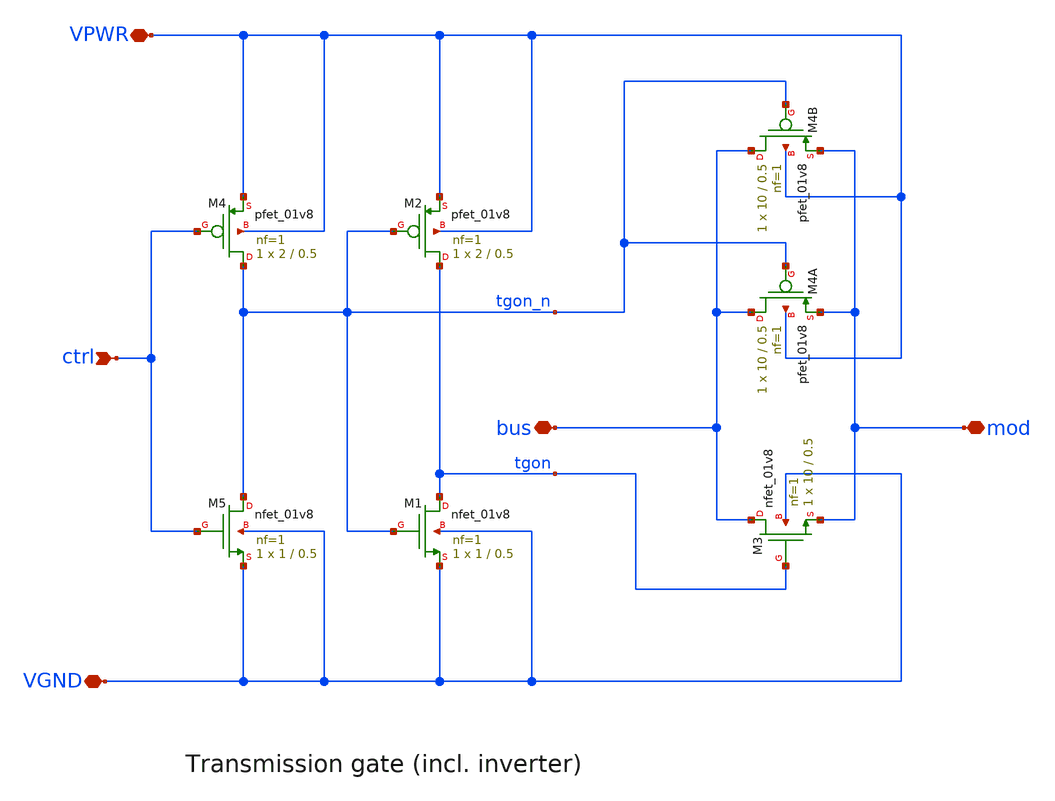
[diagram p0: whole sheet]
** sch_path: xschem/tt_asw_1v8.sch
**.subckt tt_asw_1v8 VPWR VGND mod bus ctrl
*.iopin VPWR
*.iopin VGND
*.iopin mod
*.iopin bus
*.ipin ctrl
XM3 bus tgon mod VGND sky130_fd_pr__nfet_01v8 L=0.5 W=10 nf=1 ad='int((nf+1)/2) * W/nf * 0.29' as='int((nf+2)/2) * W/nf * 0.29'
+ pd='2*int((nf+1)/2) * (W/nf + 0.29)' ps='2*int((nf+2)/2) * (W/nf + 0.29)' nrd='0.29 / W' nrs='0.29 / W'
+ sa=0 sb=0 sd=0 mult=1 m=1
XM4A bus tgon_n mod VPWR sky130_fd_pr__pfet_01v8 L=0.5 W=10 nf=1 ad='int((nf+1)/2) * W/nf * 0.29' as='int((nf+2)/2) * W/nf * 0.29'
+ pd='2*int((nf+1)/2) * (W/nf + 0.29)' ps='2*int((nf+2)/2) * (W/nf + 0.29)' nrd='0.29 / W' nrs='0.29 / W'
+ sa=0 sb=0 sd=0 mult=1 m=1
XM4B bus tgon_n mod VPWR sky130_fd_pr__pfet_01v8 L=0.5 W=10 nf=1 ad='int((nf+1)/2) * W/nf * 0.29' as='int((nf+2)/2) * W/nf * 0.29'
+ pd='2*int((nf+1)/2) * (W/nf + 0.29)' ps='2*int((nf+2)/2) * (W/nf + 0.29)' nrd='0.29 / W' nrs='0.29 / W'
+ sa=0 sb=0 sd=0 mult=1 m=1
XM1 tgon tgon_n VGND VGND sky130_fd_pr__nfet_01v8 L=0.5 W=1 nf=1 ad='int((nf+1)/2) * W/nf * 0.29' as='int((nf+2)/2) * W/nf * 0.29'
+ pd='2*int((nf+1)/2) * (W/nf + 0.29)' ps='2*int((nf+2)/2) * (W/nf + 0.29)' nrd='0.29 / W' nrs='0.29 / W'
+ sa=0 sb=0 sd=0 mult=1 m=1
XM2 tgon tgon_n VPWR VPWR sky130_fd_pr__pfet_01v8 L=0.5 W=2 nf=1 ad='int((nf+1)/2) * W/nf * 0.29' as='int((nf+2)/2) * W/nf * 0.29'
+ pd='2*int((nf+1)/2) * (W/nf + 0.29)' ps='2*int((nf+2)/2) * (W/nf + 0.29)' nrd='0.29 / W' nrs='0.29 / W'
+ sa=0 sb=0 sd=0 mult=1 m=1
XM5 tgon_n ctrl VGND VGND sky130_fd_pr__nfet_01v8 L=0.5 W=1 nf=1 ad='int((nf+1)/2) * W/nf * 0.29' as='int((nf+2)/2) * W/nf * 0.29'
+ pd='2*int((nf+1)/2) * (W/nf + 0.29)' ps='2*int((nf+2)/2) * (W/nf + 0.29)' nrd='0.29 / W' nrs='0.29 / W'
+ sa=0 sb=0 sd=0 mult=1 m=1
XM4 tgon_n ctrl VPWR VPWR sky130_fd_pr__pfet_01v8 L=0.5 W=2 nf=1 ad='int((nf+1)/2) * W/nf * 0.29' as='int((nf+2)/2) * W/nf * 0.29'
+ pd='2*int((nf+1)/2) * (W/nf + 0.29)' ps='2*int((nf+2)/2) * (W/nf + 0.29)' nrd='0.29 / W' nrs='0.29 / W'
+ sa=0 sb=0 sd=0 mult=1 m=1
**.ends
.end
